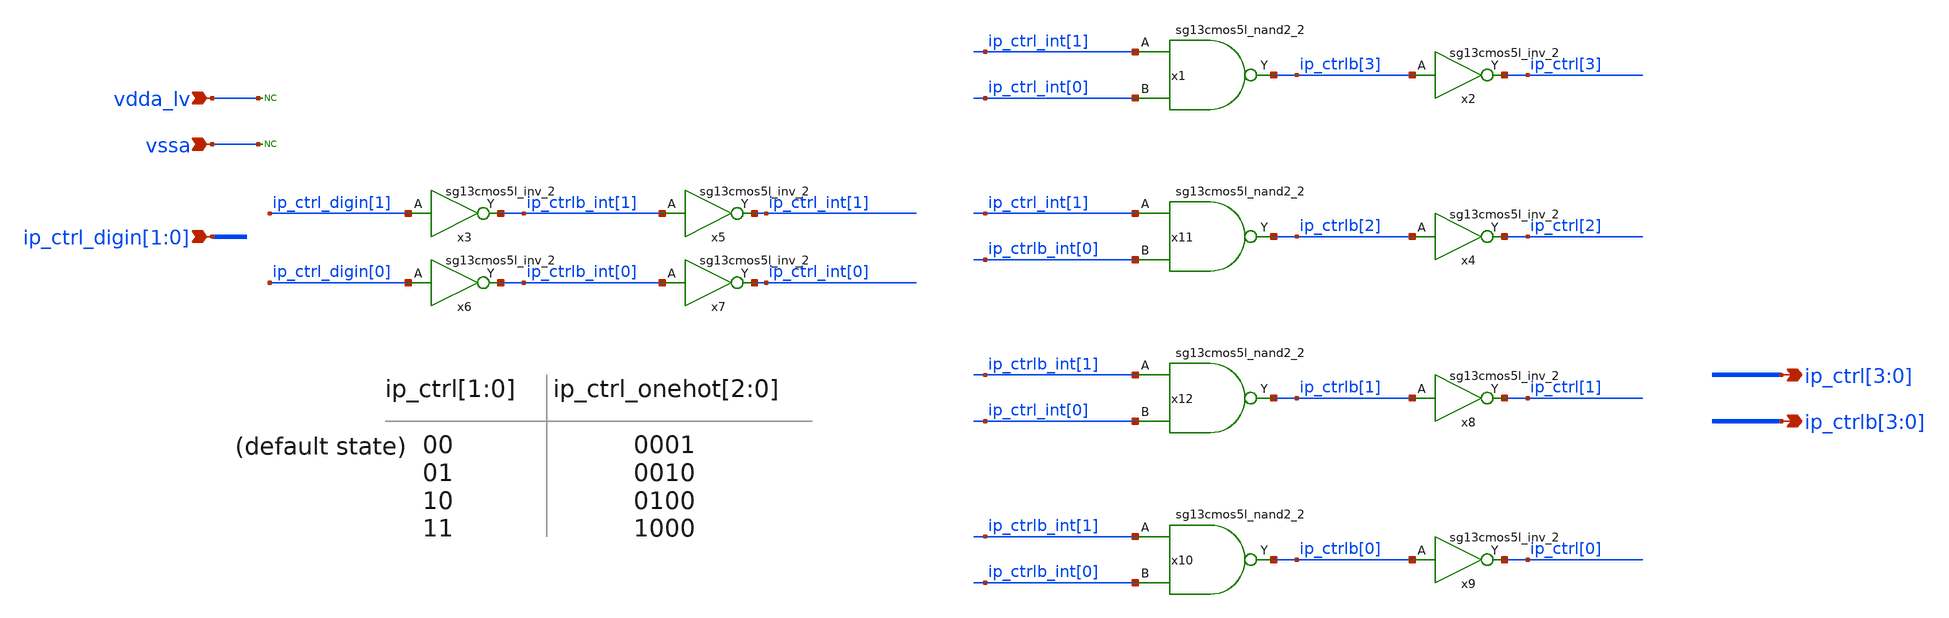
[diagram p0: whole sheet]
** sch_path: Schematics_Layout/sunrise_ip_ctrl/sunrise_ip_ctrl.sch
**.subckt sunrise_ip_ctrl ip_ctrl_digin[1],ip_ctrl_digin[0]
*+ ip_ctrl[3],ip_ctrl[2],ip_ctrl[1],ip_ctrl[0] vdda_lv vssa ip_ctrlb[3],ip_ctrlb[2],ip_ctrlb[1],ip_ctrlb[0]
*.ipin ip_ctrl_digin[1],ip_ctrl_digin[0]
*.opin ip_ctrl[3],ip_ctrl[2],ip_ctrl[1],ip_ctrl[0]
*.ipin vdda_lv
*.ipin vssa
*.opin ip_ctrlb[3],ip_ctrlb[2],ip_ctrlb[1],ip_ctrlb[0]
* noconn vdda_lv
* noconn vssa
x3 ip_ctrlb_int[1] ip_ctrl_digin[1] vdda_lv vssa sg13cmos5l_inv_2
x5 ip_ctrl_int[1] ip_ctrlb_int[1] vdda_lv vssa sg13cmos5l_inv_2
x6 ip_ctrlb_int[0] ip_ctrl_digin[0] vdda_lv vssa sg13cmos5l_inv_2
x7 ip_ctrl_int[0] ip_ctrlb_int[0] vdda_lv vssa sg13cmos5l_inv_2
x1 ip_ctrlb[3] ip_ctrl_int[1] ip_ctrl_int[0] vdda_lv vssa sg13cmos5l_nand2_2
x2 ip_ctrl[3] ip_ctrlb[3] vdda_lv vssa sg13cmos5l_inv_2
x4 ip_ctrl[2] ip_ctrlb[2] vdda_lv vssa sg13cmos5l_inv_2
x8 ip_ctrl[1] ip_ctrlb[1] vdda_lv vssa sg13cmos5l_inv_2
x11 ip_ctrlb[2] ip_ctrl_int[1] ip_ctrlb_int[0] vdda_lv vssa sg13cmos5l_nand2_2
x12 ip_ctrlb[1] ip_ctrlb_int[1] ip_ctrl_int[0] vdda_lv vssa sg13cmos5l_nand2_2
x9 ip_ctrl[0] ip_ctrlb[0] vdda_lv vssa sg13cmos5l_inv_2
x10 ip_ctrlb[0] ip_ctrlb_int[1] ip_ctrlb_int[0] vdda_lv vssa sg13cmos5l_nand2_2
**.ends
.end
